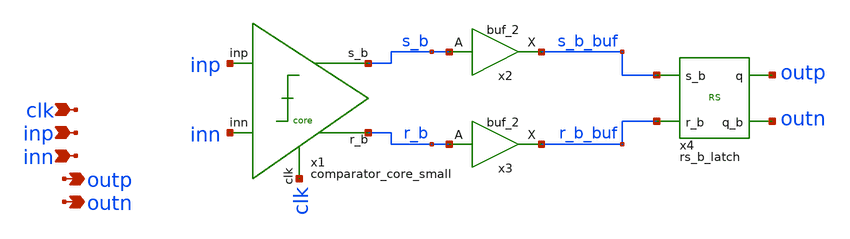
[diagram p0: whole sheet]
** sch_path: design/schematic/comparator.sch
**.subckt comparator clk inp inn outp outn
*.ipin clk
*.ipin inp
*.ipin inn
*.opin outp
*.opin outn
x1 inp inn s_b clk r_b VDD GND comparator_core_small
x2 s_b GND GND VDD VDD s_b_buf sky130_fd_sc_hd__buf_2
x3 r_b GND GND VDD VDD r_b_buf sky130_fd_sc_hd__buf_2
x4 s_b_buf r_b_buf outp outn VDD GND rs_b_latch
**.ends
.end
